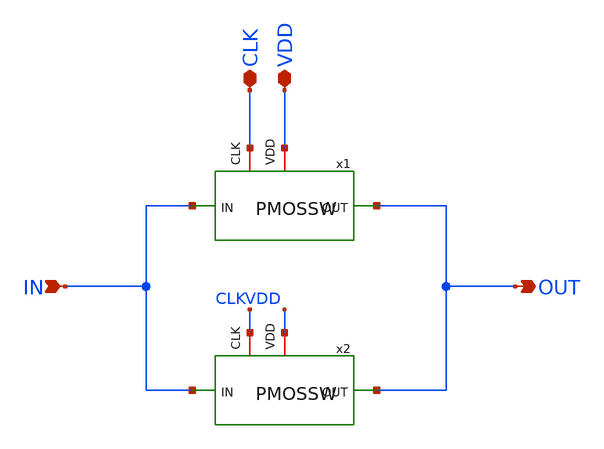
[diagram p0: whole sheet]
** sch_path: PMOSSW2.sch
**.subckt PMOSSW2 IN OUT CLK VDD
*.ipin IN
*.opin OUT
*.iopin CLK
*.iopin VDD
x1 CLK OUT IN VDD PMOSSW
x2 CLK OUT IN VDD PMOSSW
**.ends

* expanding   symbol:  PMOSSW.sym # of pins=4
** sym_path: PMOSSW.sym
** sch_path: PMOSSW.sch
.subckt PMOSSW CLK OUT IN VDD
*.ipin IN
*.opin OUT
*.iopin VDD
*.iopin CLK
M5 OUT CLK IN VDD pch w=10u l=0.35u as=0 ps=0 ad=0 pd=0 m=1
.ends

.end
